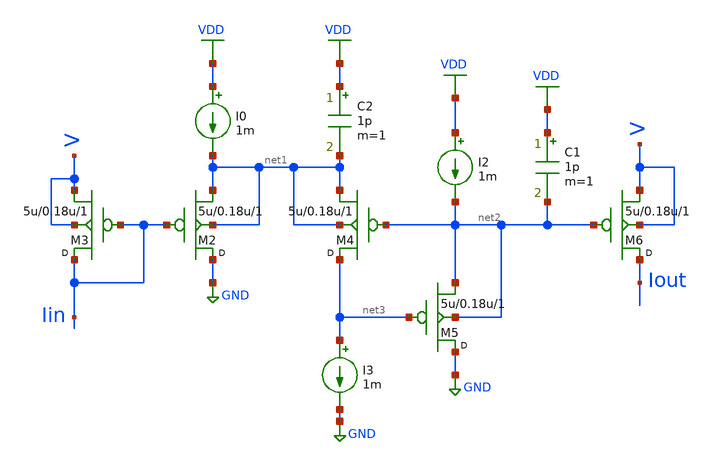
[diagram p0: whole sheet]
** sch_path: seven_peak.sch
**.subckt seven_peak
M2 GND Iin net1 net1 pmos w=5u l=0.18u m=1
M3 Iin Iin V V pmos w=5u l=0.18u m=1
M4 net3 net2 net1 net1 pmos w=5u l=0.18u m=1
M5 GND net3 net2 net2 pmos w=5u l=0.18u m=1
M6 Iout net2 V V pmos w=5u l=0.18u m=1
I0 VDD net1 1m
C1 VDD net2 1p m=1
I2 VDD net2 1m
C2 VDD net1 1p m=1
I3 net3 GND 1m
**.ends
.GLOBAL GND
.GLOBAL VDD
.end
